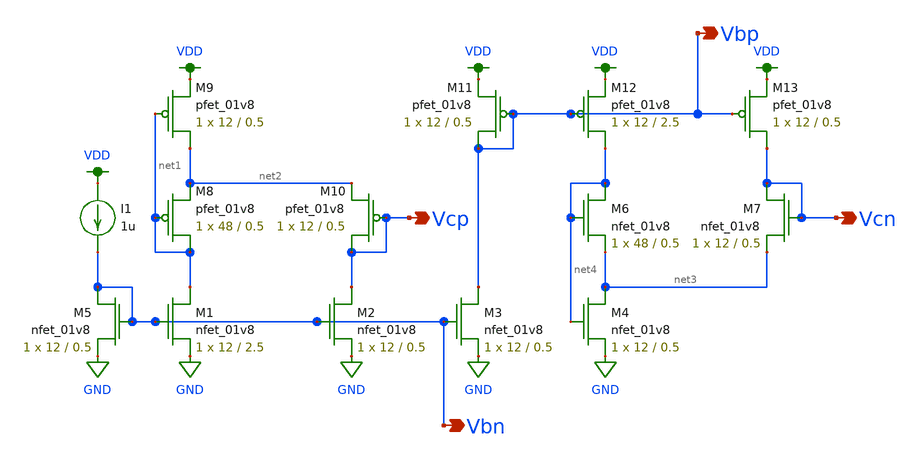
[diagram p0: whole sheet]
** sch_path: mp3/schematics/bias.sch
**.subckt bias Vcp Vcn Vbn Vbp
*.opin Vcp
*.opin Vcn
*.opin Vbn
*.opin Vbp
XM1 net1 Vbn GND GND sky130_fd_pr__nfet_01v8 L=2.5 W=12 nf=1 ad='int((nf+1)/2) * W/nf * 0.29' as='int((nf+2)/2) * W/nf * 0.29'
+ pd='2*int((nf+1)/2) * (W/nf + 0.29)' ps='2*int((nf+2)/2) * (W/nf + 0.29)' nrd='0.29 / W' nrs='0.29 / W'
+ sa=0 sb=0 sd=0 mult=1 m=1
XM2 Vcp Vbn GND GND sky130_fd_pr__nfet_01v8 L=0.5 W=12 nf=1 ad='int((nf+1)/2) * W/nf * 0.29' as='int((nf+2)/2) * W/nf * 0.29'
+ pd='2*int((nf+1)/2) * (W/nf + 0.29)' ps='2*int((nf+2)/2) * (W/nf + 0.29)' nrd='0.29 / W' nrs='0.29 / W'
+ sa=0 sb=0 sd=0 mult=1 m=1
XM3 Vbp Vbn GND GND sky130_fd_pr__nfet_01v8 L=0.5 W=12 nf=1 ad='int((nf+1)/2) * W/nf * 0.29' as='int((nf+2)/2) * W/nf * 0.29'
+ pd='2*int((nf+1)/2) * (W/nf + 0.29)' ps='2*int((nf+2)/2) * (W/nf + 0.29)' nrd='0.29 / W' nrs='0.29 / W'
+ sa=0 sb=0 sd=0 mult=1 m=1
XM4 net3 net4 GND GND sky130_fd_pr__nfet_01v8 L=0.5 W=12 nf=1 ad='int((nf+1)/2) * W/nf * 0.29' as='int((nf+2)/2) * W/nf * 0.29'
+ pd='2*int((nf+1)/2) * (W/nf + 0.29)' ps='2*int((nf+2)/2) * (W/nf + 0.29)' nrd='0.29 / W' nrs='0.29 / W'
+ sa=0 sb=0 sd=0 mult=1 m=1
XM5 Vbn Vbn GND GND sky130_fd_pr__nfet_01v8 L=0.5 W=12 nf=1 ad='int((nf+1)/2) * W/nf * 0.29' as='int((nf+2)/2) * W/nf * 0.29'
+ pd='2*int((nf+1)/2) * (W/nf + 0.29)' ps='2*int((nf+2)/2) * (W/nf + 0.29)' nrd='0.29 / W' nrs='0.29 / W'
+ sa=0 sb=0 sd=0 mult=1 m=1
XM6 net4 net4 net3 GND sky130_fd_pr__nfet_01v8 L=0.5 W=48 nf=1 ad='int((nf+1)/2) * W/nf * 0.29' as='int((nf+2)/2) * W/nf * 0.29'
+ pd='2*int((nf+1)/2) * (W/nf + 0.29)' ps='2*int((nf+2)/2) * (W/nf + 0.29)' nrd='0.29 / W' nrs='0.29 / W'
+ sa=0 sb=0 sd=0 mult=1 m=1
XM7 Vcn Vcn net3 GND sky130_fd_pr__nfet_01v8 L=0.5 W=12 nf=1 ad='int((nf+1)/2) * W/nf * 0.29' as='int((nf+2)/2) * W/nf * 0.29'
+ pd='2*int((nf+1)/2) * (W/nf + 0.29)' ps='2*int((nf+2)/2) * (W/nf + 0.29)' nrd='0.29 / W' nrs='0.29 / W'
+ sa=0 sb=0 sd=0 mult=1 m=1
XM8 net1 net1 net2 VDD sky130_fd_pr__pfet_01v8 L=0.5 W=48 nf=1 ad='int((nf+1)/2) * W/nf * 0.29' as='int((nf+2)/2) * W/nf * 0.29'
+ pd='2*int((nf+1)/2) * (W/nf + 0.29)' ps='2*int((nf+2)/2) * (W/nf + 0.29)' nrd='0.29 / W' nrs='0.29 / W'
+ sa=0 sb=0 sd=0 mult=1 m=1
XM9 net2 net1 VDD VDD sky130_fd_pr__pfet_01v8 L=0.5 W=12 nf=1 ad='int((nf+1)/2) * W/nf * 0.29' as='int((nf+2)/2) * W/nf * 0.29'
+ pd='2*int((nf+1)/2) * (W/nf + 0.29)' ps='2*int((nf+2)/2) * (W/nf + 0.29)' nrd='0.29 / W' nrs='0.29 / W'
+ sa=0 sb=0 sd=0 mult=1 m=1
XM10 Vcp Vcp net2 VDD sky130_fd_pr__pfet_01v8 L=0.5 W=12 nf=1 ad='int((nf+1)/2) * W/nf * 0.29' as='int((nf+2)/2) * W/nf * 0.29'
+ pd='2*int((nf+1)/2) * (W/nf + 0.29)' ps='2*int((nf+2)/2) * (W/nf + 0.29)' nrd='0.29 / W' nrs='0.29 / W'
+ sa=0 sb=0 sd=0 mult=1 m=1
XM11 Vbp Vbp VDD VDD sky130_fd_pr__pfet_01v8 L=0.5 W=12 nf=1 ad='int((nf+1)/2) * W/nf * 0.29' as='int((nf+2)/2) * W/nf * 0.29'
+ pd='2*int((nf+1)/2) * (W/nf + 0.29)' ps='2*int((nf+2)/2) * (W/nf + 0.29)' nrd='0.29 / W' nrs='0.29 / W'
+ sa=0 sb=0 sd=0 mult=1 m=1
XM12 net4 Vbp VDD VDD sky130_fd_pr__pfet_01v8 L=2.5 W=12 nf=1 ad='int((nf+1)/2) * W/nf * 0.29' as='int((nf+2)/2) * W/nf * 0.29'
+ pd='2*int((nf+1)/2) * (W/nf + 0.29)' ps='2*int((nf+2)/2) * (W/nf + 0.29)' nrd='0.29 / W' nrs='0.29 / W'
+ sa=0 sb=0 sd=0 mult=1 m=1
XM13 Vcn Vbp VDD VDD sky130_fd_pr__pfet_01v8 L=0.5 W=12 nf=1 ad='int((nf+1)/2) * W/nf * 0.29' as='int((nf+2)/2) * W/nf * 0.29'
+ pd='2*int((nf+1)/2) * (W/nf + 0.29)' ps='2*int((nf+2)/2) * (W/nf + 0.29)' nrd='0.29 / W' nrs='0.29 / W'
+ sa=0 sb=0 sd=0 mult=1 m=1
I1 VDD Vbn 1u
**.ends
.GLOBAL GND
.GLOBAL VDD
.end
